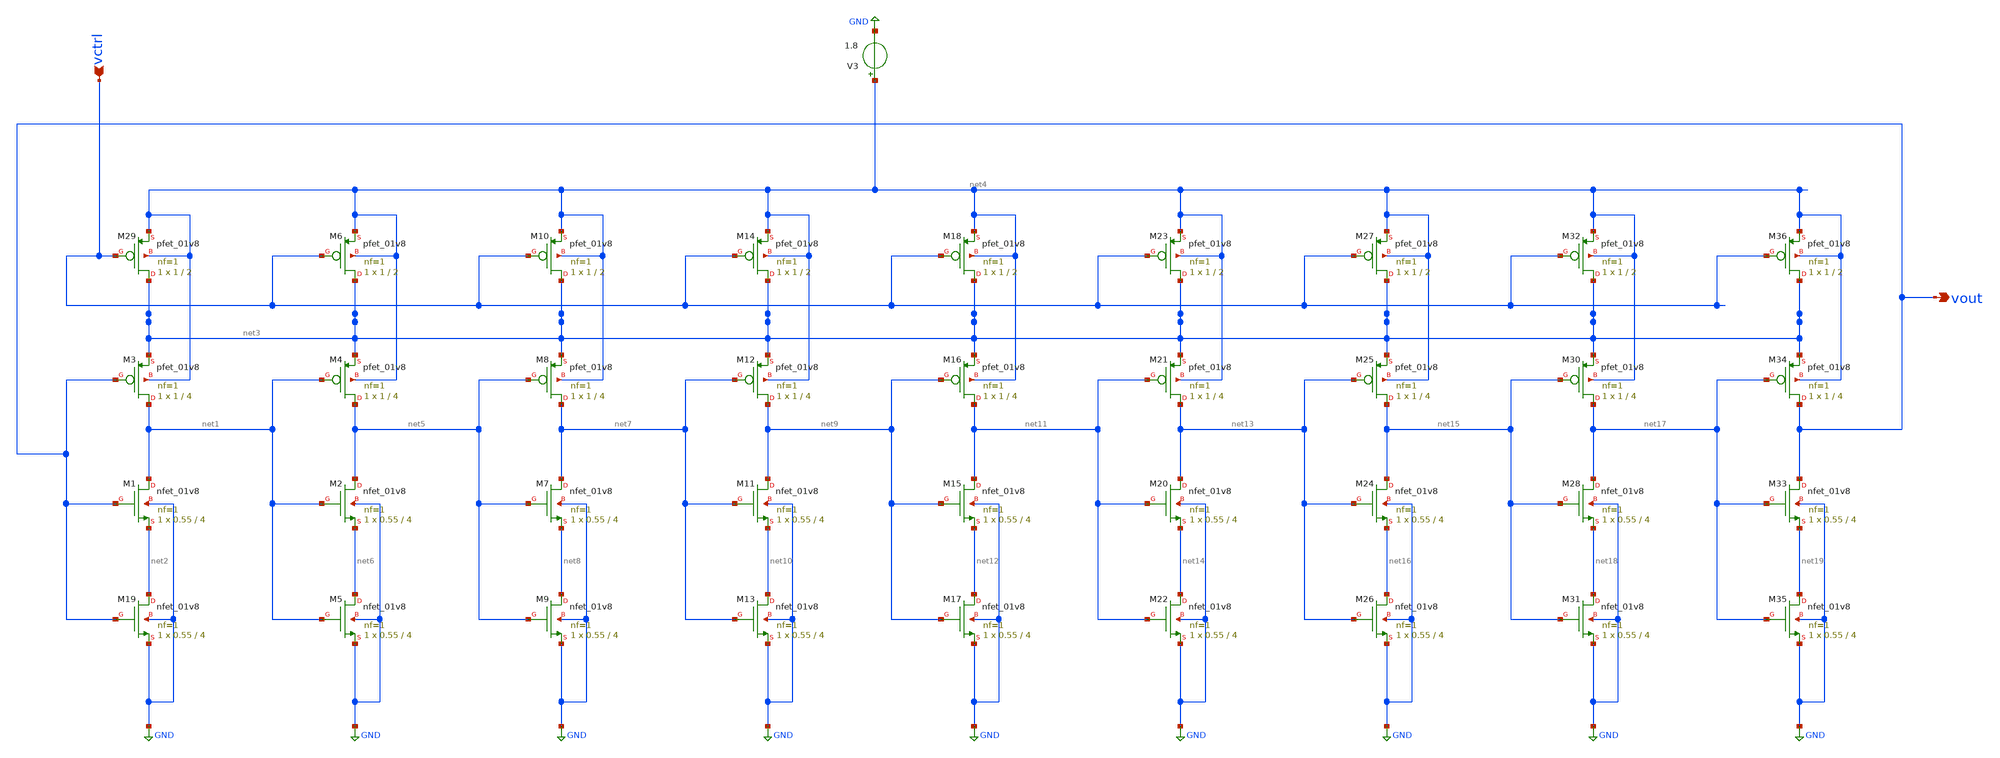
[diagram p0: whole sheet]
** sch_path: osc.sch
**.subckt osc vctrl vout
*.ipin vctrl
*.opin vout
XM1 net1 vout net2 GND sky130_fd_pr__nfet_01v8 L=4 W=0.55 nf=1 ad='int((nf+1)/2) * W/nf * 0.29' as='int((nf+2)/2) * W/nf * 0.29'
+ pd='2*int((nf+1)/2) * (W/nf + 0.29)' ps='2*int((nf+2)/2) * (W/nf + 0.29)' nrd='0.29 / W' nrs='0.29 / W'
+ sa=0 sb=0 sd=0 mult=1 m=1
XM3 net1 vout net3 net4 sky130_fd_pr__pfet_01v8 L=4 W=1 nf=1 ad='int((nf+1)/2) * W/nf * 0.29' as='int((nf+2)/2) * W/nf * 0.29'
+ pd='2*int((nf+1)/2) * (W/nf + 0.29)' ps='2*int((nf+2)/2) * (W/nf + 0.29)' nrd='0.29 / W' nrs='0.29 / W'
+ sa=0 sb=0 sd=0 mult=1 m=1
XM19 net2 vout GND GND sky130_fd_pr__nfet_01v8 L=4 W=0.55 nf=1 ad='int((nf+1)/2) * W/nf * 0.29' as='int((nf+2)/2) * W/nf * 0.29'
+ pd='2*int((nf+1)/2) * (W/nf + 0.29)' ps='2*int((nf+2)/2) * (W/nf + 0.29)' nrd='0.29 / W' nrs='0.29 / W'
+ sa=0 sb=0 sd=0 mult=1 m=1
XM29 net3 vctrl net4 net4 sky130_fd_pr__pfet_01v8 L=2 W=1 nf=1 ad='int((nf+1)/2) * W/nf * 0.29' as='int((nf+2)/2) * W/nf * 0.29'
+ pd='2*int((nf+1)/2) * (W/nf + 0.29)' ps='2*int((nf+2)/2) * (W/nf + 0.29)' nrd='0.29 / W' nrs='0.29 / W'
+ sa=0 sb=0 sd=0 mult=1 m=1
V3 net4 GND 1.8
XM2 net5 net1 net6 GND sky130_fd_pr__nfet_01v8 L=4 W=0.55 nf=1 ad='int((nf+1)/2) * W/nf * 0.29' as='int((nf+2)/2) * W/nf * 0.29'
+ pd='2*int((nf+1)/2) * (W/nf + 0.29)' ps='2*int((nf+2)/2) * (W/nf + 0.29)' nrd='0.29 / W' nrs='0.29 / W'
+ sa=0 sb=0 sd=0 mult=1 m=1
XM4 net5 net1 net3 net4 sky130_fd_pr__pfet_01v8 L=4 W=1 nf=1 ad='int((nf+1)/2) * W/nf * 0.29' as='int((nf+2)/2) * W/nf * 0.29'
+ pd='2*int((nf+1)/2) * (W/nf + 0.29)' ps='2*int((nf+2)/2) * (W/nf + 0.29)' nrd='0.29 / W' nrs='0.29 / W'
+ sa=0 sb=0 sd=0 mult=1 m=1
XM5 net6 net1 GND GND sky130_fd_pr__nfet_01v8 L=4 W=0.55 nf=1 ad='int((nf+1)/2) * W/nf * 0.29' as='int((nf+2)/2) * W/nf * 0.29'
+ pd='2*int((nf+1)/2) * (W/nf + 0.29)' ps='2*int((nf+2)/2) * (W/nf + 0.29)' nrd='0.29 / W' nrs='0.29 / W'
+ sa=0 sb=0 sd=0 mult=1 m=1
XM6 net3 vctrl net4 net4 sky130_fd_pr__pfet_01v8 L=2 W=1 nf=1 ad='int((nf+1)/2) * W/nf * 0.29' as='int((nf+2)/2) * W/nf * 0.29'
+ pd='2*int((nf+1)/2) * (W/nf + 0.29)' ps='2*int((nf+2)/2) * (W/nf + 0.29)' nrd='0.29 / W' nrs='0.29 / W'
+ sa=0 sb=0 sd=0 mult=1 m=1
XM7 net7 net5 net8 GND sky130_fd_pr__nfet_01v8 L=4 W=0.55 nf=1 ad='int((nf+1)/2) * W/nf * 0.29' as='int((nf+2)/2) * W/nf * 0.29'
+ pd='2*int((nf+1)/2) * (W/nf + 0.29)' ps='2*int((nf+2)/2) * (W/nf + 0.29)' nrd='0.29 / W' nrs='0.29 / W'
+ sa=0 sb=0 sd=0 mult=1 m=1
XM8 net7 net5 net3 net4 sky130_fd_pr__pfet_01v8 L=4 W=1 nf=1 ad='int((nf+1)/2) * W/nf * 0.29' as='int((nf+2)/2) * W/nf * 0.29'
+ pd='2*int((nf+1)/2) * (W/nf + 0.29)' ps='2*int((nf+2)/2) * (W/nf + 0.29)' nrd='0.29 / W' nrs='0.29 / W'
+ sa=0 sb=0 sd=0 mult=1 m=1
XM9 net8 net5 GND GND sky130_fd_pr__nfet_01v8 L=4 W=0.55 nf=1 ad='int((nf+1)/2) * W/nf * 0.29' as='int((nf+2)/2) * W/nf * 0.29'
+ pd='2*int((nf+1)/2) * (W/nf + 0.29)' ps='2*int((nf+2)/2) * (W/nf + 0.29)' nrd='0.29 / W' nrs='0.29 / W'
+ sa=0 sb=0 sd=0 mult=1 m=1
XM10 net3 vctrl net4 net4 sky130_fd_pr__pfet_01v8 L=2 W=1 nf=1 ad='int((nf+1)/2) * W/nf * 0.29' as='int((nf+2)/2) * W/nf * 0.29'
+ pd='2*int((nf+1)/2) * (W/nf + 0.29)' ps='2*int((nf+2)/2) * (W/nf + 0.29)' nrd='0.29 / W' nrs='0.29 / W'
+ sa=0 sb=0 sd=0 mult=1 m=1
XM11 net9 net7 net10 GND sky130_fd_pr__nfet_01v8 L=4 W=0.55 nf=1 ad='int((nf+1)/2) * W/nf * 0.29' as='int((nf+2)/2) * W/nf * 0.29'
+ pd='2*int((nf+1)/2) * (W/nf + 0.29)' ps='2*int((nf+2)/2) * (W/nf + 0.29)' nrd='0.29 / W' nrs='0.29 / W'
+ sa=0 sb=0 sd=0 mult=1 m=1
XM12 net9 net7 net3 net4 sky130_fd_pr__pfet_01v8 L=4 W=1 nf=1 ad='int((nf+1)/2) * W/nf * 0.29' as='int((nf+2)/2) * W/nf * 0.29'
+ pd='2*int((nf+1)/2) * (W/nf + 0.29)' ps='2*int((nf+2)/2) * (W/nf + 0.29)' nrd='0.29 / W' nrs='0.29 / W'
+ sa=0 sb=0 sd=0 mult=1 m=1
XM13 net10 net7 GND GND sky130_fd_pr__nfet_01v8 L=4 W=0.55 nf=1 ad='int((nf+1)/2) * W/nf * 0.29' as='int((nf+2)/2) * W/nf * 0.29'
+ pd='2*int((nf+1)/2) * (W/nf + 0.29)' ps='2*int((nf+2)/2) * (W/nf + 0.29)' nrd='0.29 / W' nrs='0.29 / W'
+ sa=0 sb=0 sd=0 mult=1 m=1
XM14 net3 vctrl net4 net4 sky130_fd_pr__pfet_01v8 L=2 W=1 nf=1 ad='int((nf+1)/2) * W/nf * 0.29' as='int((nf+2)/2) * W/nf * 0.29'
+ pd='2*int((nf+1)/2) * (W/nf + 0.29)' ps='2*int((nf+2)/2) * (W/nf + 0.29)' nrd='0.29 / W' nrs='0.29 / W'
+ sa=0 sb=0 sd=0 mult=1 m=1
XM15 net11 net9 net12 GND sky130_fd_pr__nfet_01v8 L=4 W=0.55 nf=1 ad='int((nf+1)/2) * W/nf * 0.29' as='int((nf+2)/2) * W/nf * 0.29'
+ pd='2*int((nf+1)/2) * (W/nf + 0.29)' ps='2*int((nf+2)/2) * (W/nf + 0.29)' nrd='0.29 / W' nrs='0.29 / W'
+ sa=0 sb=0 sd=0 mult=1 m=1
XM16 net11 net9 net3 net4 sky130_fd_pr__pfet_01v8 L=4 W=1 nf=1 ad='int((nf+1)/2) * W/nf * 0.29' as='int((nf+2)/2) * W/nf * 0.29'
+ pd='2*int((nf+1)/2) * (W/nf + 0.29)' ps='2*int((nf+2)/2) * (W/nf + 0.29)' nrd='0.29 / W' nrs='0.29 / W'
+ sa=0 sb=0 sd=0 mult=1 m=1
XM17 net12 net9 GND GND sky130_fd_pr__nfet_01v8 L=4 W=0.55 nf=1 ad='int((nf+1)/2) * W/nf * 0.29' as='int((nf+2)/2) * W/nf * 0.29'
+ pd='2*int((nf+1)/2) * (W/nf + 0.29)' ps='2*int((nf+2)/2) * (W/nf + 0.29)' nrd='0.29 / W' nrs='0.29 / W'
+ sa=0 sb=0 sd=0 mult=1 m=1
XM18 net3 vctrl net4 net4 sky130_fd_pr__pfet_01v8 L=2 W=1 nf=1 ad='int((nf+1)/2) * W/nf * 0.29' as='int((nf+2)/2) * W/nf * 0.29'
+ pd='2*int((nf+1)/2) * (W/nf + 0.29)' ps='2*int((nf+2)/2) * (W/nf + 0.29)' nrd='0.29 / W' nrs='0.29 / W'
+ sa=0 sb=0 sd=0 mult=1 m=1
XM20 net13 net11 net14 GND sky130_fd_pr__nfet_01v8 L=4 W=0.55 nf=1 ad='int((nf+1)/2) * W/nf * 0.29' as='int((nf+2)/2) * W/nf * 0.29'
+ pd='2*int((nf+1)/2) * (W/nf + 0.29)' ps='2*int((nf+2)/2) * (W/nf + 0.29)' nrd='0.29 / W' nrs='0.29 / W'
+ sa=0 sb=0 sd=0 mult=1 m=1
XM21 net13 net11 net3 net4 sky130_fd_pr__pfet_01v8 L=4 W=1 nf=1 ad='int((nf+1)/2) * W/nf * 0.29' as='int((nf+2)/2) * W/nf * 0.29'
+ pd='2*int((nf+1)/2) * (W/nf + 0.29)' ps='2*int((nf+2)/2) * (W/nf + 0.29)' nrd='0.29 / W' nrs='0.29 / W'
+ sa=0 sb=0 sd=0 mult=1 m=1
XM22 net14 net11 GND GND sky130_fd_pr__nfet_01v8 L=4 W=0.55 nf=1 ad='int((nf+1)/2) * W/nf * 0.29' as='int((nf+2)/2) * W/nf * 0.29'
+ pd='2*int((nf+1)/2) * (W/nf + 0.29)' ps='2*int((nf+2)/2) * (W/nf + 0.29)' nrd='0.29 / W' nrs='0.29 / W'
+ sa=0 sb=0 sd=0 mult=1 m=1
XM23 net3 vctrl net4 net4 sky130_fd_pr__pfet_01v8 L=2 W=1 nf=1 ad='int((nf+1)/2) * W/nf * 0.29' as='int((nf+2)/2) * W/nf * 0.29'
+ pd='2*int((nf+1)/2) * (W/nf + 0.29)' ps='2*int((nf+2)/2) * (W/nf + 0.29)' nrd='0.29 / W' nrs='0.29 / W'
+ sa=0 sb=0 sd=0 mult=1 m=1
XM24 net15 net13 net16 GND sky130_fd_pr__nfet_01v8 L=4 W=0.55 nf=1 ad='int((nf+1)/2) * W/nf * 0.29' as='int((nf+2)/2) * W/nf * 0.29'
+ pd='2*int((nf+1)/2) * (W/nf + 0.29)' ps='2*int((nf+2)/2) * (W/nf + 0.29)' nrd='0.29 / W' nrs='0.29 / W'
+ sa=0 sb=0 sd=0 mult=1 m=1
XM25 net15 net13 net3 net4 sky130_fd_pr__pfet_01v8 L=4 W=1 nf=1 ad='int((nf+1)/2) * W/nf * 0.29' as='int((nf+2)/2) * W/nf * 0.29'
+ pd='2*int((nf+1)/2) * (W/nf + 0.29)' ps='2*int((nf+2)/2) * (W/nf + 0.29)' nrd='0.29 / W' nrs='0.29 / W'
+ sa=0 sb=0 sd=0 mult=1 m=1
XM26 net16 net13 GND GND sky130_fd_pr__nfet_01v8 L=4 W=0.55 nf=1 ad='int((nf+1)/2) * W/nf * 0.29' as='int((nf+2)/2) * W/nf * 0.29'
+ pd='2*int((nf+1)/2) * (W/nf + 0.29)' ps='2*int((nf+2)/2) * (W/nf + 0.29)' nrd='0.29 / W' nrs='0.29 / W'
+ sa=0 sb=0 sd=0 mult=1 m=1
XM27 net3 vctrl net4 net4 sky130_fd_pr__pfet_01v8 L=2 W=1 nf=1 ad='int((nf+1)/2) * W/nf * 0.29' as='int((nf+2)/2) * W/nf * 0.29'
+ pd='2*int((nf+1)/2) * (W/nf + 0.29)' ps='2*int((nf+2)/2) * (W/nf + 0.29)' nrd='0.29 / W' nrs='0.29 / W'
+ sa=0 sb=0 sd=0 mult=1 m=1
XM28 net17 net15 net18 GND sky130_fd_pr__nfet_01v8 L=4 W=0.55 nf=1 ad='int((nf+1)/2) * W/nf * 0.29' as='int((nf+2)/2) * W/nf * 0.29'
+ pd='2*int((nf+1)/2) * (W/nf + 0.29)' ps='2*int((nf+2)/2) * (W/nf + 0.29)' nrd='0.29 / W' nrs='0.29 / W'
+ sa=0 sb=0 sd=0 mult=1 m=1
XM30 net17 net15 net3 net4 sky130_fd_pr__pfet_01v8 L=4 W=1 nf=1 ad='int((nf+1)/2) * W/nf * 0.29' as='int((nf+2)/2) * W/nf * 0.29'
+ pd='2*int((nf+1)/2) * (W/nf + 0.29)' ps='2*int((nf+2)/2) * (W/nf + 0.29)' nrd='0.29 / W' nrs='0.29 / W'
+ sa=0 sb=0 sd=0 mult=1 m=1
XM31 net18 net15 GND GND sky130_fd_pr__nfet_01v8 L=4 W=0.55 nf=1 ad='int((nf+1)/2) * W/nf * 0.29' as='int((nf+2)/2) * W/nf * 0.29'
+ pd='2*int((nf+1)/2) * (W/nf + 0.29)' ps='2*int((nf+2)/2) * (W/nf + 0.29)' nrd='0.29 / W' nrs='0.29 / W'
+ sa=0 sb=0 sd=0 mult=1 m=1
XM32 net3 vctrl net4 net4 sky130_fd_pr__pfet_01v8 L=2 W=1 nf=1 ad='int((nf+1)/2) * W/nf * 0.29' as='int((nf+2)/2) * W/nf * 0.29'
+ pd='2*int((nf+1)/2) * (W/nf + 0.29)' ps='2*int((nf+2)/2) * (W/nf + 0.29)' nrd='0.29 / W' nrs='0.29 / W'
+ sa=0 sb=0 sd=0 mult=1 m=1
XM33 vout net17 net19 GND sky130_fd_pr__nfet_01v8 L=4 W=0.55 nf=1 ad='int((nf+1)/2) * W/nf * 0.29' as='int((nf+2)/2) * W/nf * 0.29'
+ pd='2*int((nf+1)/2) * (W/nf + 0.29)' ps='2*int((nf+2)/2) * (W/nf + 0.29)' nrd='0.29 / W' nrs='0.29 / W'
+ sa=0 sb=0 sd=0 mult=1 m=1
XM34 vout net17 net3 net4 sky130_fd_pr__pfet_01v8 L=4 W=1 nf=1 ad='int((nf+1)/2) * W/nf * 0.29' as='int((nf+2)/2) * W/nf * 0.29'
+ pd='2*int((nf+1)/2) * (W/nf + 0.29)' ps='2*int((nf+2)/2) * (W/nf + 0.29)' nrd='0.29 / W' nrs='0.29 / W'
+ sa=0 sb=0 sd=0 mult=1 m=1
XM35 net19 net17 GND GND sky130_fd_pr__nfet_01v8 L=4 W=0.55 nf=1 ad='int((nf+1)/2) * W/nf * 0.29' as='int((nf+2)/2) * W/nf * 0.29'
+ pd='2*int((nf+1)/2) * (W/nf + 0.29)' ps='2*int((nf+2)/2) * (W/nf + 0.29)' nrd='0.29 / W' nrs='0.29 / W'
+ sa=0 sb=0 sd=0 mult=1 m=1
XM36 net3 vctrl net4 net4 sky130_fd_pr__pfet_01v8 L=2 W=1 nf=1 ad='int((nf+1)/2) * W/nf * 0.29' as='int((nf+2)/2) * W/nf * 0.29'
+ pd='2*int((nf+1)/2) * (W/nf + 0.29)' ps='2*int((nf+2)/2) * (W/nf + 0.29)' nrd='0.29 / W' nrs='0.29 / W'
+ sa=0 sb=0 sd=0 mult=1 m=1
**.ends
.GLOBAL GND
.end
